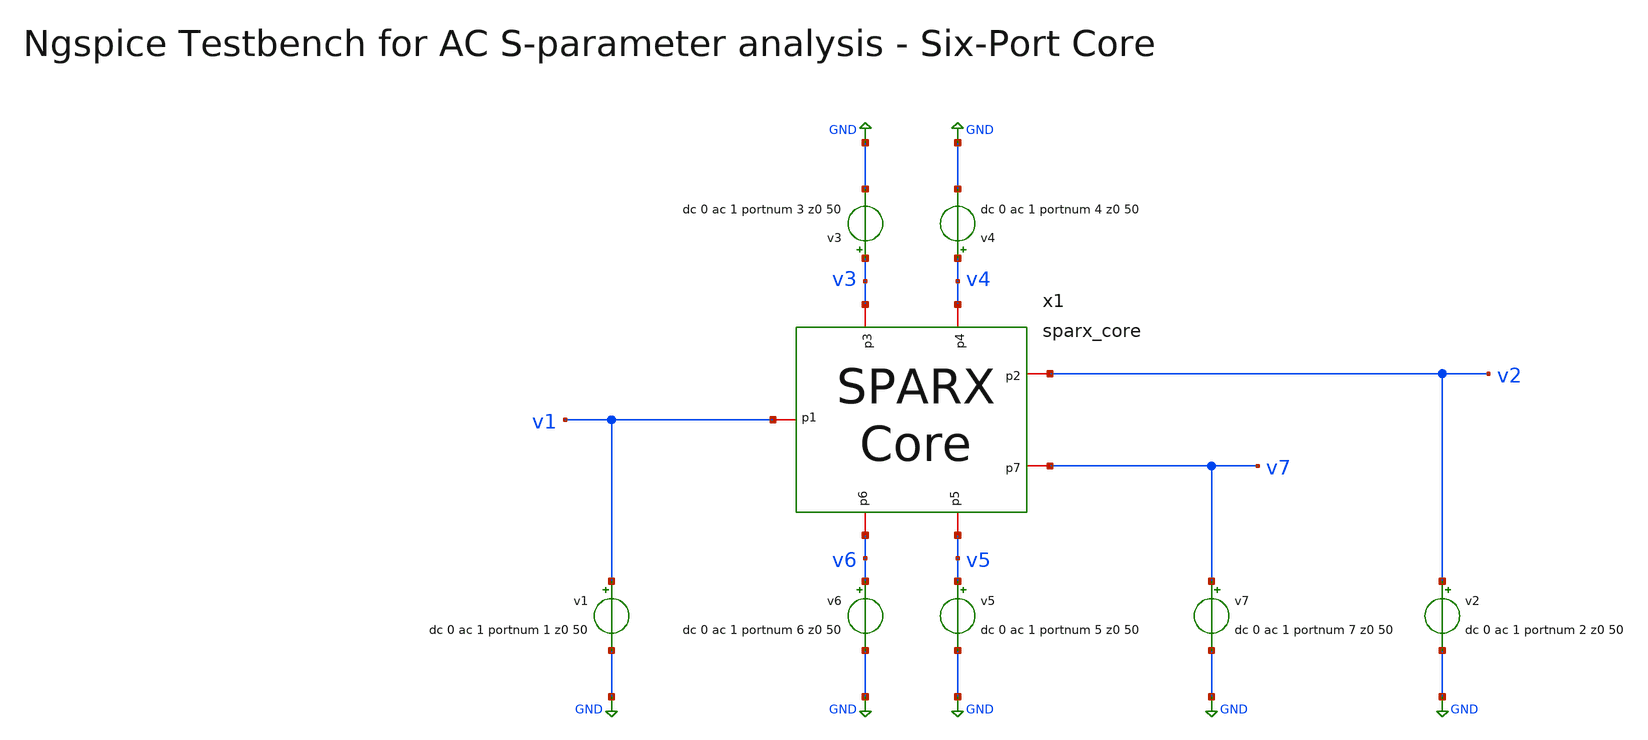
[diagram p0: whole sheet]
** sch_path: testbenches/sparx_core_tb_acsp_ngspice.sch
* schematic/sparx_core.sch:
* SPDX-FileCopyrightText: 2025-2026 The SPARX Team
* SPDX-License-Identifier: Apache-2.0 WITH SHL-2.1
**.subckt sparx_core_tb_acsp_ngspice
v7 v7 GND dc 0 ac 1 portnum 7 z0 50
v2 v2 GND dc 0 ac 1 portnum 2 z0 50
x1 v3 v4 v2 v1 v7 v5 v6 sparx_core
v6 v6 GND dc 0 ac 1 portnum 6 z0 50
v5 v5 GND dc 0 ac 1 portnum 5 z0 50
v1 v1 GND dc 0 ac 1 portnum 1 z0 50
v4 v4 GND dc 0 ac 1 portnum 4 z0 50
v3 v3 GND dc 0 ac 1 portnum 3 z0 50
**** begin user architecture code


.include ../../netlist/spice/sparx_bpf_le.spice
.include ../../netlist/spice/sparx_wpd_le.spice
.include ../../netlist/spice/sparx_blc_le.spice
.include ../sim_range.spice
.param temp=27
.options savecurrents klu method=gear reltol=1e-3 abstol=1e-15 gmin=1e-15
.control

save all

set wr_vecnames
set wr_singlescale

* User Constants
* f_min / f_max come from ../sim_range.spice (.csparam),
* auto-synced to the loaded Touchstone by snp2le.
* edit that file for a standalone run.

* Operating Point Analysis
op
remzerovec
write @schname\.raw
set appendwrite

* AC S-Parameter Analysis
sp lin 1001 $&const.f_min $&const.f_max
remzerovec

* Calculating S-Parameters
let s31_dB = db(S_3_1)
let s41_dB = db(S_4_1)
let s51_dB = db(S_5_1)
let s61_dB = db(S_6_1)
let s32_dB = db(S_3_2)
let s42_dB = db(S_4_2)
let s52_dB = db(S_5_2)
let s62_dB = db(S_6_2)
let s11_dB = db(S_1_1)
let s22_dB = db(S_2_2)
let s33_dB = db(s_3_3)
let s44_dB = db(S_4_4)
let s55_dB = db(S_5_5)
let s66_dB = db(S_6_6)
let s77_dB = db(S_7_7)
let s41_31_dB = s41_dB - s31_dB
let s51_61_dB = s51_dB - s61_dB
let s32_42_dB = s32_dB - s42_dB
let s62_52_dB = s62_dB - s52_dB

let s31_deg = cph(S_3_1) * 180/pi
let s41_deg = cph(S_4_1) * 180/pi
let s51_deg = cph(S_5_1) * 180/pi
let s61_deg = cph(S_6_1) * 180/pi
let s32_deg = cph(S_3_2) * 180/pi
let s42_deg = cph(S_4_2) * 180/pi
let s52_deg = cph(S_5_2) * 180/pi
let s62_deg = cph(S_6_2) * 180/pi
let s11_deg = cph(S_1_1) * 180/pi
let s22_deg = cph(S_2_2) * 180/pi
let s33_deg = cph(s_3_3) * 180/pi
let s44_deg = cph(S_4_4) * 180/pi
let s55_deg = cph(S_5_5) * 180/pi
let s66_deg = cph(S_6_6) * 180/pi
let s77_deg = cph(S_7_7) * 180/pi

let s41_31_deg = cph(S_4_1/S_3_1) * 180/pi
let s51_61_deg = cph(S_5_1/S_6_1) * 180/pi
let s32_42_deg = cph(S_3_2/S_4_2) * 180/pi
let s62_52_deg = cph(S_6_2/S_5_2) * 180/pi

* Write the raw AFTER the derived vectors so the interactive graphs can
* reference the imbalance vectors (s41_31_deg, ...) directly by name.
write @schname\.raw
set appendwrite

* Plotting
plot s11_dB s22_dB s33_dB s44_dB s55_dB s66_dB s77_dB
plot s41_31_dB s51_61_dB s32_42_dB s62_52_dB
plot s41_31_deg s51_61_deg s32_42_deg s62_52_deg

* Write Data
unset appendwrite
set wr_vecnames
set wr_singlescale
wrdata ../sim_data/@schname\.txt  s11_dB s22_dB s33_dB s44_dB s55_dB s66_dB s77_dB  s41_31_dB
+ s51_61_dB s32_42_dB s62_52_dB  s41_31_deg s51_61_deg s32_42_deg s62_52_deg

*quit
.endc



.lib cornerMOSlv.lib mos_tt
.lib cornerMOShv.lib mos_tt
.lib cornerHBT.lib hbt_typ
.lib cornerRES.lib res_typ
.lib cornerCAP.lib cap_typ
.lib cornerDIO.lib dio_tt

**** end user architecture code
**.ends

* expanding   symbol:  sparx_core.sym # of pins=7
** sym_path: schematic/sparx_core.sym
** sch_path: schematic/sparx_core.sch
.subckt sparx_core p3 p4 p2 p1 p7 p5 p6
*.iopin p1
*.iopin p3
*.iopin p4
*.iopin p2
*.iopin p7
*.iopin p6
*.iopin p5
x5 net3 net1 p4 p3 sparx_blc_le
x6 p2 p7 net2 net1 sparx_blc_le
x7 net5 net4 net3 sparx_wpd_le
x8 p1 net5 sparx_bpf_le
x4 net4 net2 p5 p6 sparx_blc_le
.ends

.GLOBAL GND
.end
